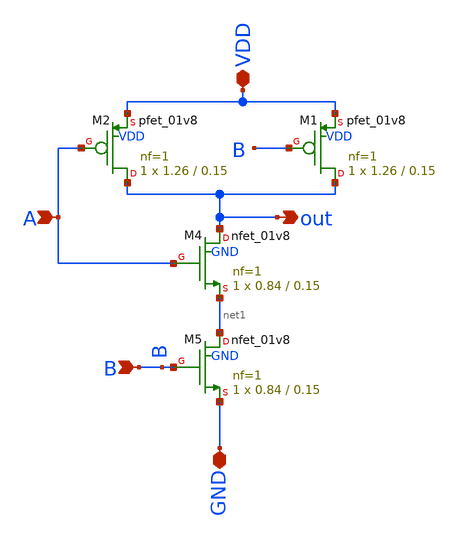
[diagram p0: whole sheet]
** sch_path: xschem/charge_pumps2/nand_gate.sch
**.subckt nand_gate GND VDD A B out
*.iopin GND
*.iopin VDD
*.ipin A
*.ipin B
*.opin out
XM2 out A VDD VDD sky130_fd_pr__pfet_01v8 L=0.15 W=1.26 nf=1 ad='int((nf+1)/2) * W/nf * 0.29' as='int((nf+2)/2) * W/nf * 0.29'
+ pd='2*int((nf+1)/2) * (W/nf + 0.29)' ps='2*int((nf+2)/2) * (W/nf + 0.29)' nrd='0.29 / W' nrs='0.29 / W'
+ sa=0 sb=0 sd=0 mult=1 m=1
XM1 out B VDD VDD sky130_fd_pr__pfet_01v8 L=0.15 W=1.26 nf=1 ad='int((nf+1)/2) * W/nf * 0.29' as='int((nf+2)/2) * W/nf * 0.29'
+ pd='2*int((nf+1)/2) * (W/nf + 0.29)' ps='2*int((nf+2)/2) * (W/nf + 0.29)' nrd='0.29 / W' nrs='0.29 / W'
+ sa=0 sb=0 sd=0 mult=1 m=1
XM4 out A net1 GND sky130_fd_pr__nfet_01v8 L=0.15 W=0.84 nf=1 ad='int((nf+1)/2) * W/nf * 0.29' as='int((nf+2)/2) * W/nf * 0.29'
+ pd='2*int((nf+1)/2) * (W/nf + 0.29)' ps='2*int((nf+2)/2) * (W/nf + 0.29)' nrd='0.29 / W' nrs='0.29 / W'
+ sa=0 sb=0 sd=0 mult=1 m=1
XM5 net1 B GND GND sky130_fd_pr__nfet_01v8 L=0.15 W=0.84 nf=1 ad='int((nf+1)/2) * W/nf * 0.29' as='int((nf+2)/2) * W/nf * 0.29'
+ pd='2*int((nf+1)/2) * (W/nf + 0.29)' ps='2*int((nf+2)/2) * (W/nf + 0.29)' nrd='0.29 / W' nrs='0.29 / W'
+ sa=0 sb=0 sd=0 mult=1 m=1
**.ends
.end
